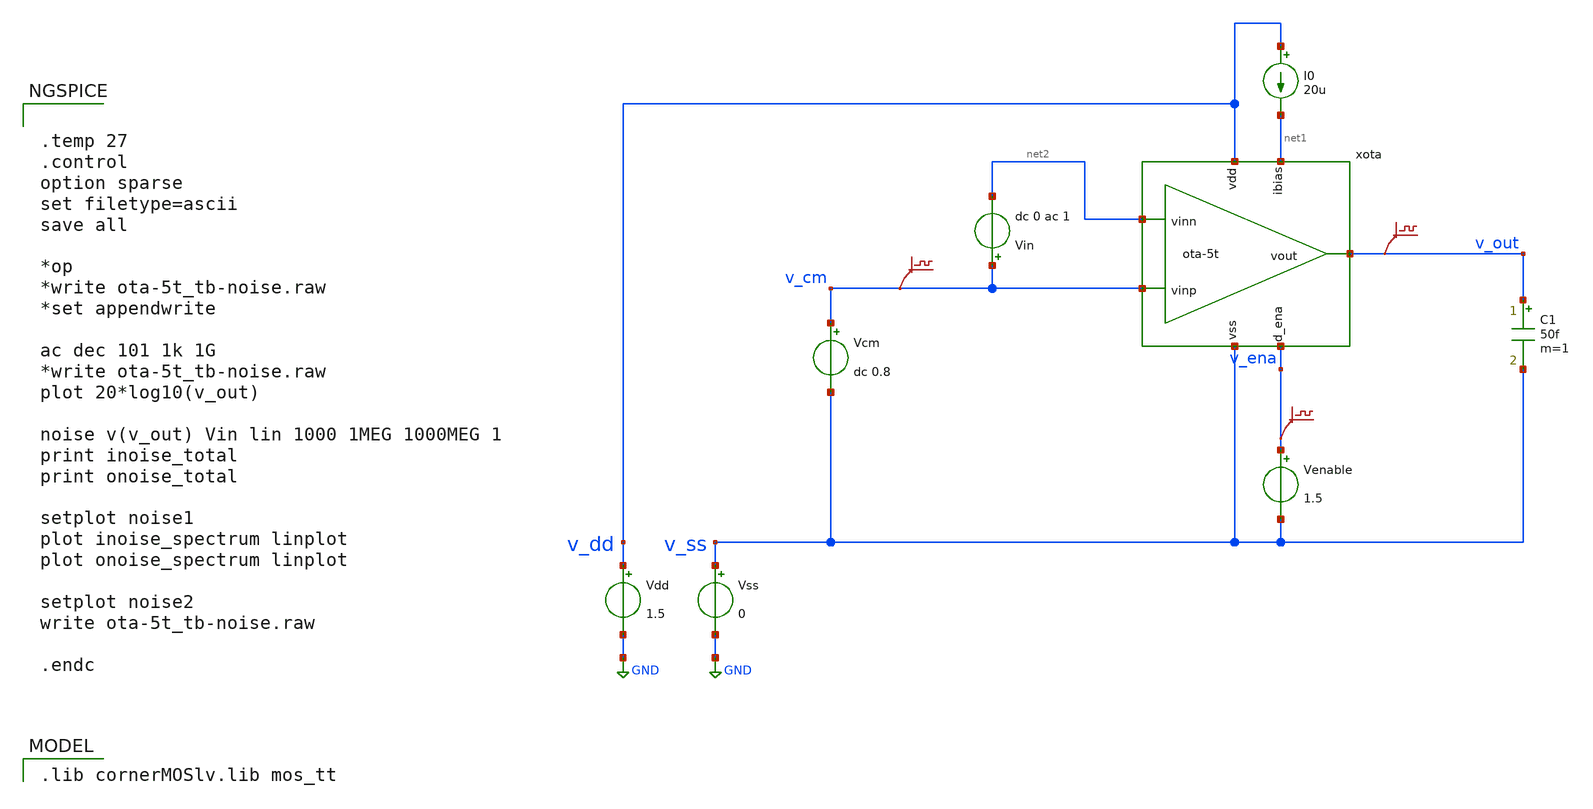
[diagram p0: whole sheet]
** sch_path: prj/template/3_Real_circuits/ota-5t_tb-noise.sch
* (c) 2024-2025 H. Pretl, Apache-2.0 license
**.subckt ota-5t_tb-noise
Vdd v_dd GND 1.5
xota v_dd v_out net2 v_cm net1 v_ena v_ss ota-5t
Vss v_ss GND 0
C1 v_out v_ss 50f m=1
Vcm v_cm v_ss dc 0.8
I0 v_dd net1 20u
Venable v_ena v_ss 1.5
.save v(v_cm)
.save v(v_out)
.save v(v_ena)
Vin v_cm net2 dc 0 ac 1
**** begin user architecture code
 .lib cornerMOSlv.lib mos_tt



.temp 27
.control
option sparse
set filetype=ascii
save all

*op
*write ota-5t_tb-noise.raw
*set appendwrite

ac dec 101 1k 1G
*write ota-5t_tb-noise.raw
plot 20*log10(v_out)

noise v(v_out) Vin lin 1000 1MEG 1000MEG 1
print inoise_total
print onoise_total

setplot noise1
plot inoise_spectrum linplot
plot onoise_spectrum linplot

setplot noise2
write ota-5t_tb-noise.raw

.endc


**** end user architecture code
**.ends

* expanding   symbol:  ota-5t.sym # of pins=7
** sym_path: prj/template/3_Real_circuits/ota-5t.sym
** sch_path: prj/template/3_Real_circuits/ota-5t.sch
.subckt ota-5t vdd vout vinn vinp ibias d_ena vss
*.ipin ibias
*.iopin vdd
*.iopin vss
*.ipin vinp
*.ipin vinn
*.opin vout
*.ipin d_ena
XM5 tail gate_n vss vss sg13_lv_nmos w=0.5u l=5u ng=1 m=1 mm_ok=1
XM4 vout gate_p vdd vdd sg13_lv_pmos w=1.5u l=5u ng=1 m=1 mm_ok=1
XM1 gate_p vinp tail vss sg13_lv_nmos w=2u l=5u ng=1 m=1 mm_ok=1
XM2 vout vinn tail vss sg13_lv_nmos w=2u l=5u ng=1 m=1 mm_ok=1
XM3 gate_p gate_p vdd vdd sg13_lv_pmos w=1.5u l=5u ng=1 m=1 mm_ok=1
XM6 ibias gate_n vss vss sg13_lv_nmos w=2.5u l=5u ng=5 m=1 mm_ok=1
XM9 gate_n ena_n vss vss sg13_lv_nmos w=0.5u l=0.13u ng=1 m=1 mm_ok=1
XM11 gate_p ena vdd vdd sg13_lv_pmos w=1.5u l=0.13u ng=1 m=1 mm_ok=1
XM7 ena ena_n vss vss sg13_lv_nmos w=0.5u l=0.13u ng=1 m=1 mm_ok=1
XM8 ena ena_n vdd vdd sg13_lv_pmos w=1.5u l=0.13u ng=1 m=1 mm_ok=1
XM10 ibias ena gate_n vss sg13_lv_nmos w=0.5u l=0.13u ng=1 m=1 mm_ok=1
XM12 ena_n d_ena vss vss sg13_lv_nmos w=0.5u l=0.13u ng=1 m=1 mm_ok=1
XM13 ena_n d_ena vdd vdd sg13_lv_pmos w=1.5u l=0.13u ng=1 m=1 mm_ok=1
.ends

.GLOBAL GND
.end
